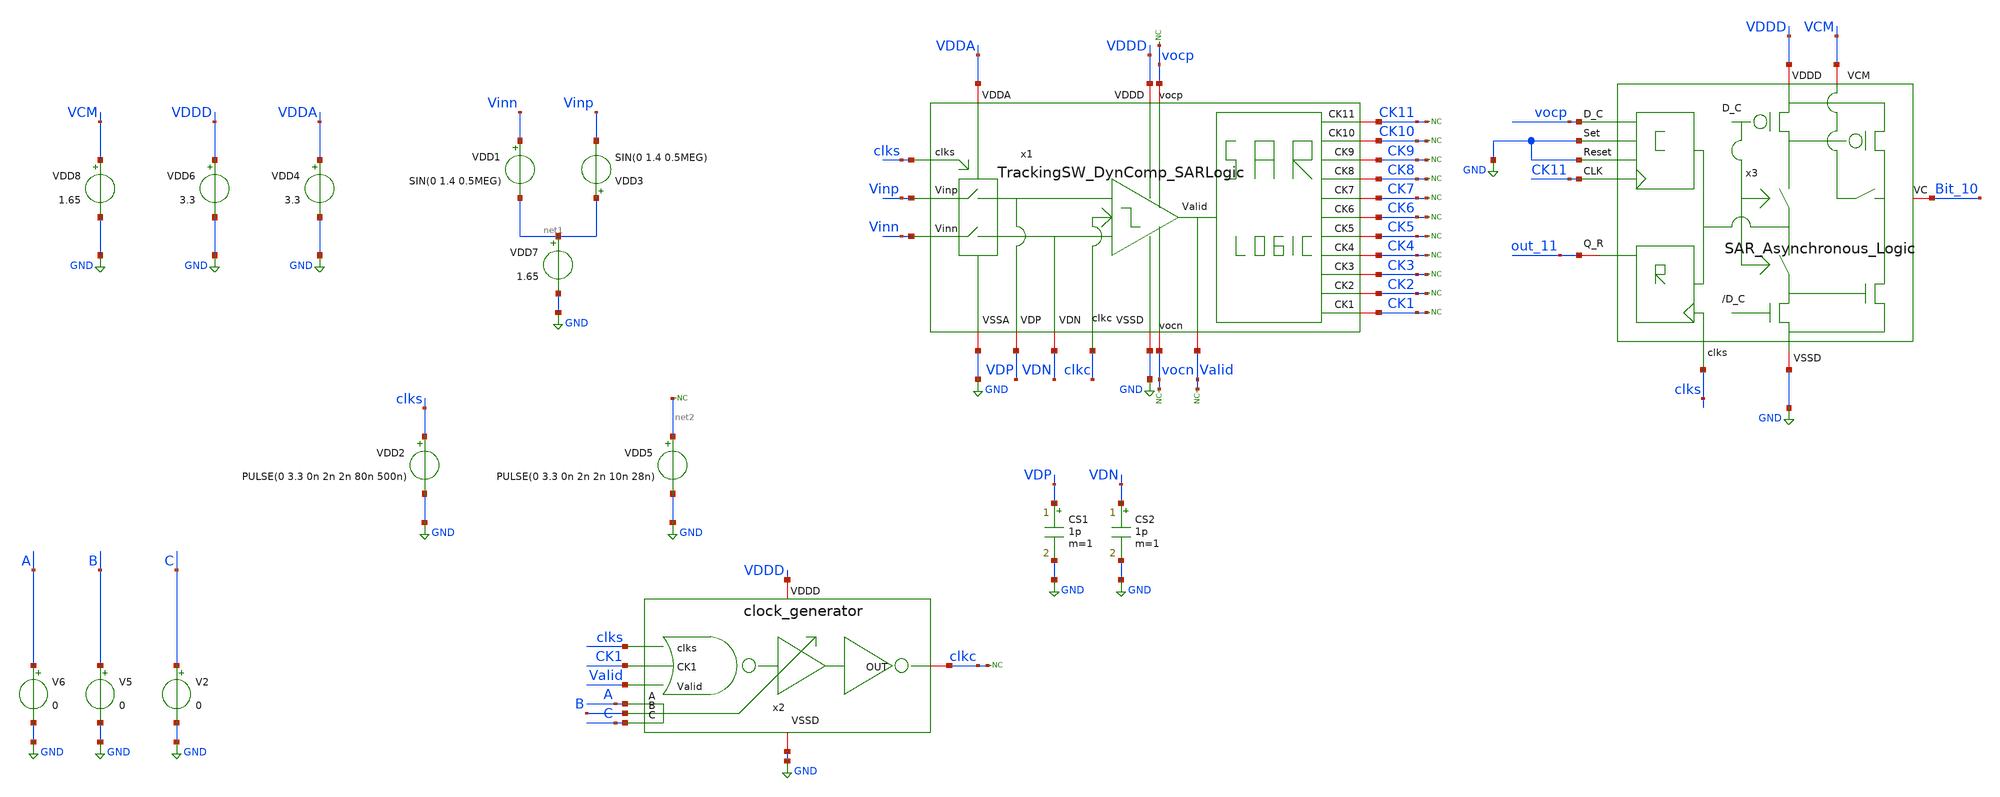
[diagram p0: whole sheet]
** sch_path: SAR_ADC/integration/TrackingSW_DynComp_SARLogic_tb.sch
**.subckt TrackingSW_DynComp_SARLogic_tb
x1 Valid vocp vocn CK11 CK10 CK9 CK8 CK7 CK6 CK5 CK4 CK3 CK2 CK1 VDDA GND VDDD GND VDP clks VDN clkc
+ Vinp Vinn TrackingSW_DynComp_SARLogic
VDD2 clks GND PULSE(0 3.3 0n 2n 2n 80n 500n)
VDD4 VDDA GND 3.3
VDD1 Vinn net1 SIN(0 1.4 0.5MEG)
VDD3 net1 Vinp SIN(0 1.4 0.5MEG)
VDD5 net2 GND PULSE(0 3.3 0n 2n 2n 10n 28n)
VDD6 VDDD GND 3.3
CS1 VDP GND 1p m=1
CS2 VDN GND 1p m=1
* noconn CK11
* noconn CK10
* noconn CK9
* noconn CK8
* noconn CK7
* noconn CK6
* noconn CK5
* noconn CK4
* noconn CK3
* noconn CK2
* noconn CK1
* noconn vocp
* noconn vocn
* noconn Valid
VDD7 net1 GND 1.65
x2 clkc VDDD GND clks CK1 Valid A B C clock_generator
* noconn clkc
* noconn #net2
V2 C GND 0
V5 B GND 0
V6 A GND 0
x3 VCM Bit_10 out_11 clks VDDD GND GND GND vocp CK11 SAR_Asynchronous_Logic
VDD8 VCM GND 1.65
**** begin user architecture code



*Parameters

.options TEMP = 50.0
.lib /home/electrica/Documents/gf180_projects/pdk/gf180mcuC/libs.tech/ngspice/sm141064.ngspice typical
.include /home/electrica/Documents/gf180_projects/pdk/gf180mcuC/libs.tech/ngspice/design.ngspice

*Data to save
.save all


* Simulation
.control
tran 0.1n 5u 0.01n
*setplot dc1
*plot V(Vinp)+40 V(Vinn)+36 V(clks)+32 V(VDP)+28 V(VDN)+28 V(.x1.x3.aN)+24 V(.x1.x3.aP)+20
*+ V(.x1.x3.dN)+16 V(.x1.x3.dP)+12 V(.x1.x3.Vocp)+8 V(.x1.x3.Vocn)+4 V(Valid)
let vin_diff = Vinp - Vinn
let vout_diff =VDP - VDN
plot v(clks)+76 v(vout_diff)+72 v(vin_diff)+72 V(.x1.x3.aN)+68 V(.x1.x3.aP)+64 V(.x1.x3.dN)+60
+ V(.x1.x3.dP)+56 V(.vocp)+52 V(.vocn)+48 V(Valid)+44 V(CK11)+40 V(CK10)+36 V(CK9)+32 V(CK8)+28 V(CK7)+24 V(CK6)+20
+ V(CK5)+16 V(CK4)+12 V(CK3)+8 V(CK2)+4 V(CK1) v(Bit_10)-4 v(out_11)-8
set filetype = ascii
write TrackingSW_DynComp_SARLogic_tb_tran.raw

reset
unset filetype
op
save all
write TrackingSW_DynComp_SARLogic_tb.raw


.endc
.end


**** end user architecture code
**.ends
.GLOBAL GND
.end
